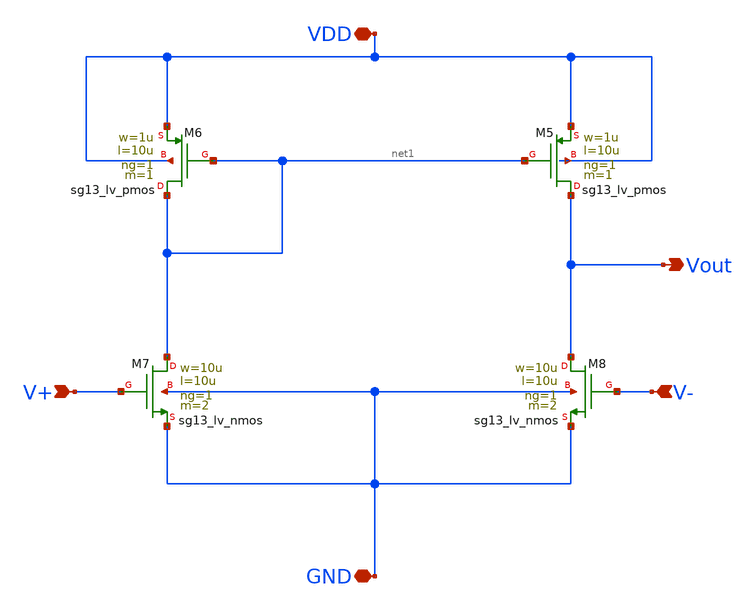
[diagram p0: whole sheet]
** sch_path: SSDOR_w_startup_1V_ihp/Ib_4u/Ib_4u_opamp/Ib_4u_opamp.sch
**.subckt Ib_4u_opamp VDD V+ V- GND Vout
*.iopin VDD
*.ipin V+
*.ipin V-
*.iopin GND
*.opin Vout
XM5 Vout net1 VDD VDD sg13_lv_pmos w=1u l=10u ng=1 m=1 mm_ok=1
XM6 net1 net1 VDD VDD sg13_lv_pmos w=1u l=10u ng=1 m=1 mm_ok=1
XM7 net1 V+ GND GND sg13_lv_nmos w=10u l=10u ng=1 m=2 mm_ok=1
XM8 Vout V- GND GND sg13_lv_nmos w=10u l=10u ng=1 m=2 mm_ok=1
**.ends
.end
